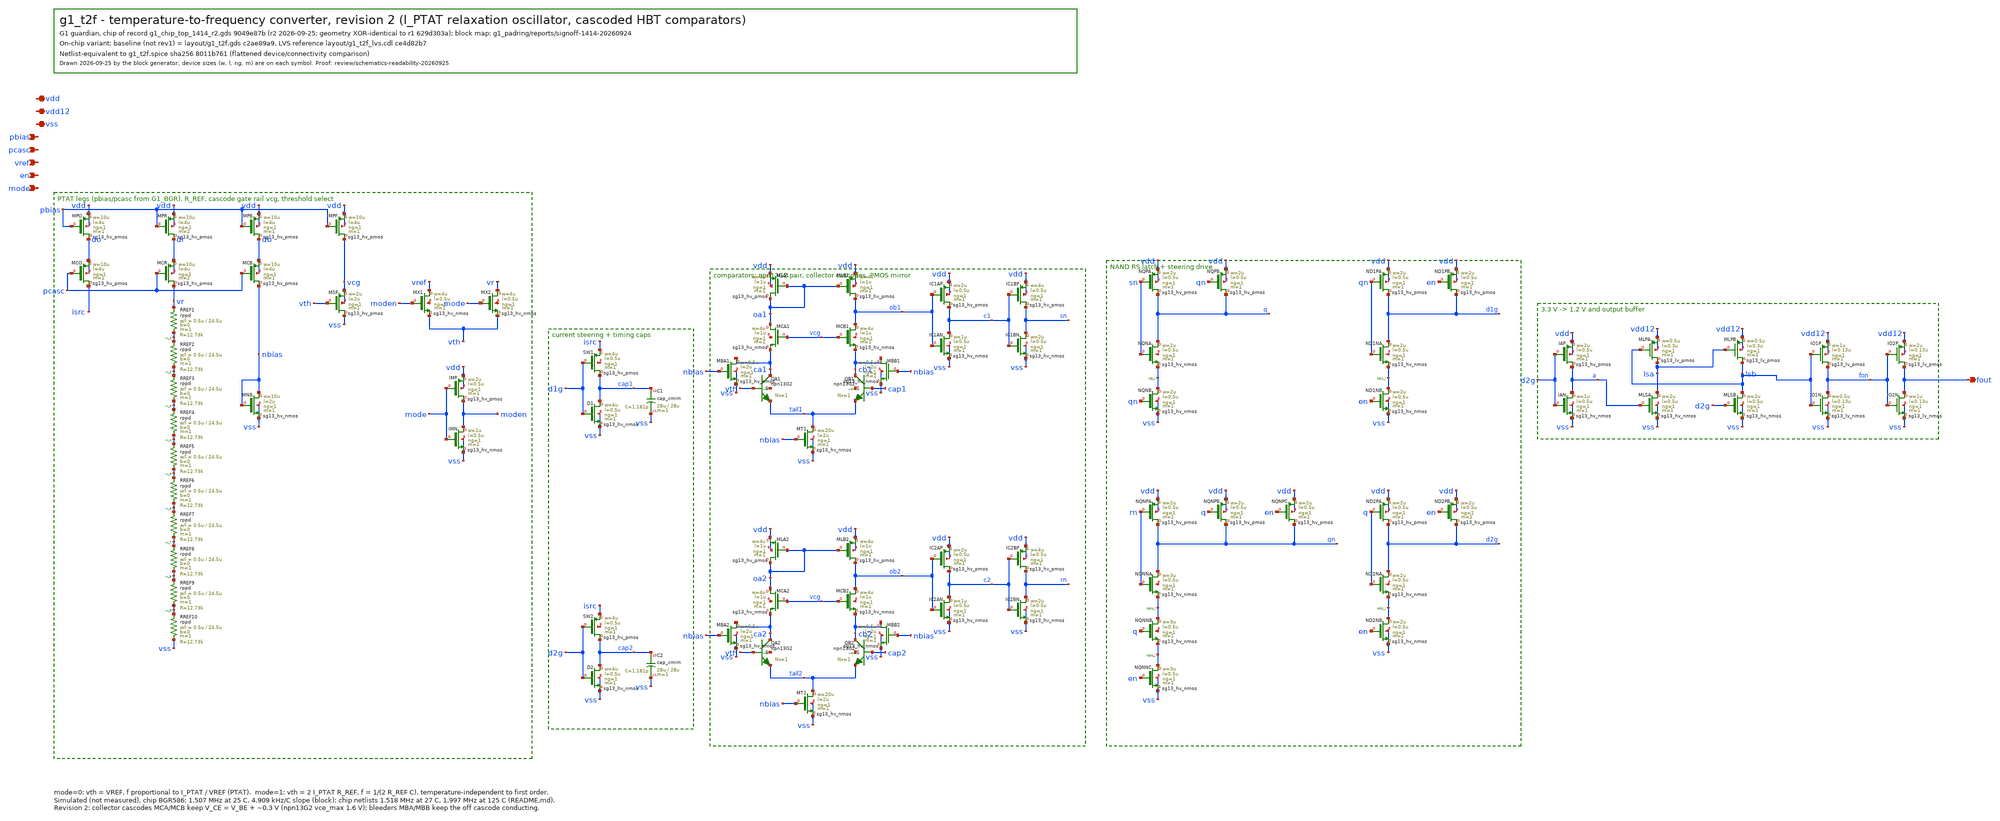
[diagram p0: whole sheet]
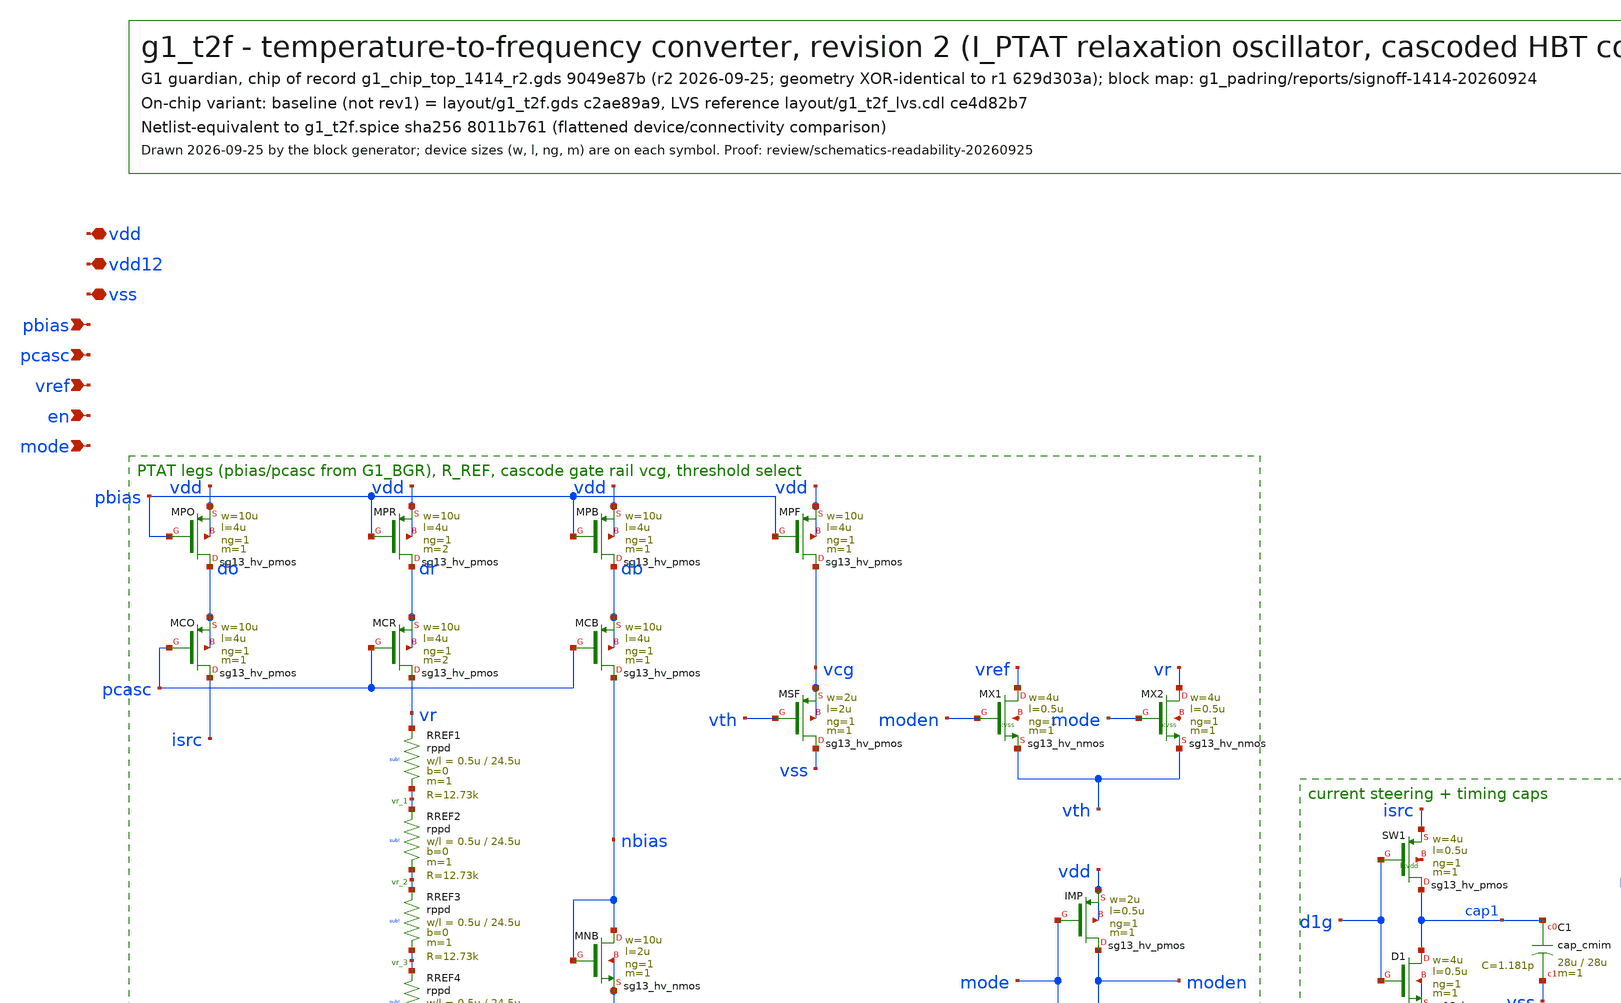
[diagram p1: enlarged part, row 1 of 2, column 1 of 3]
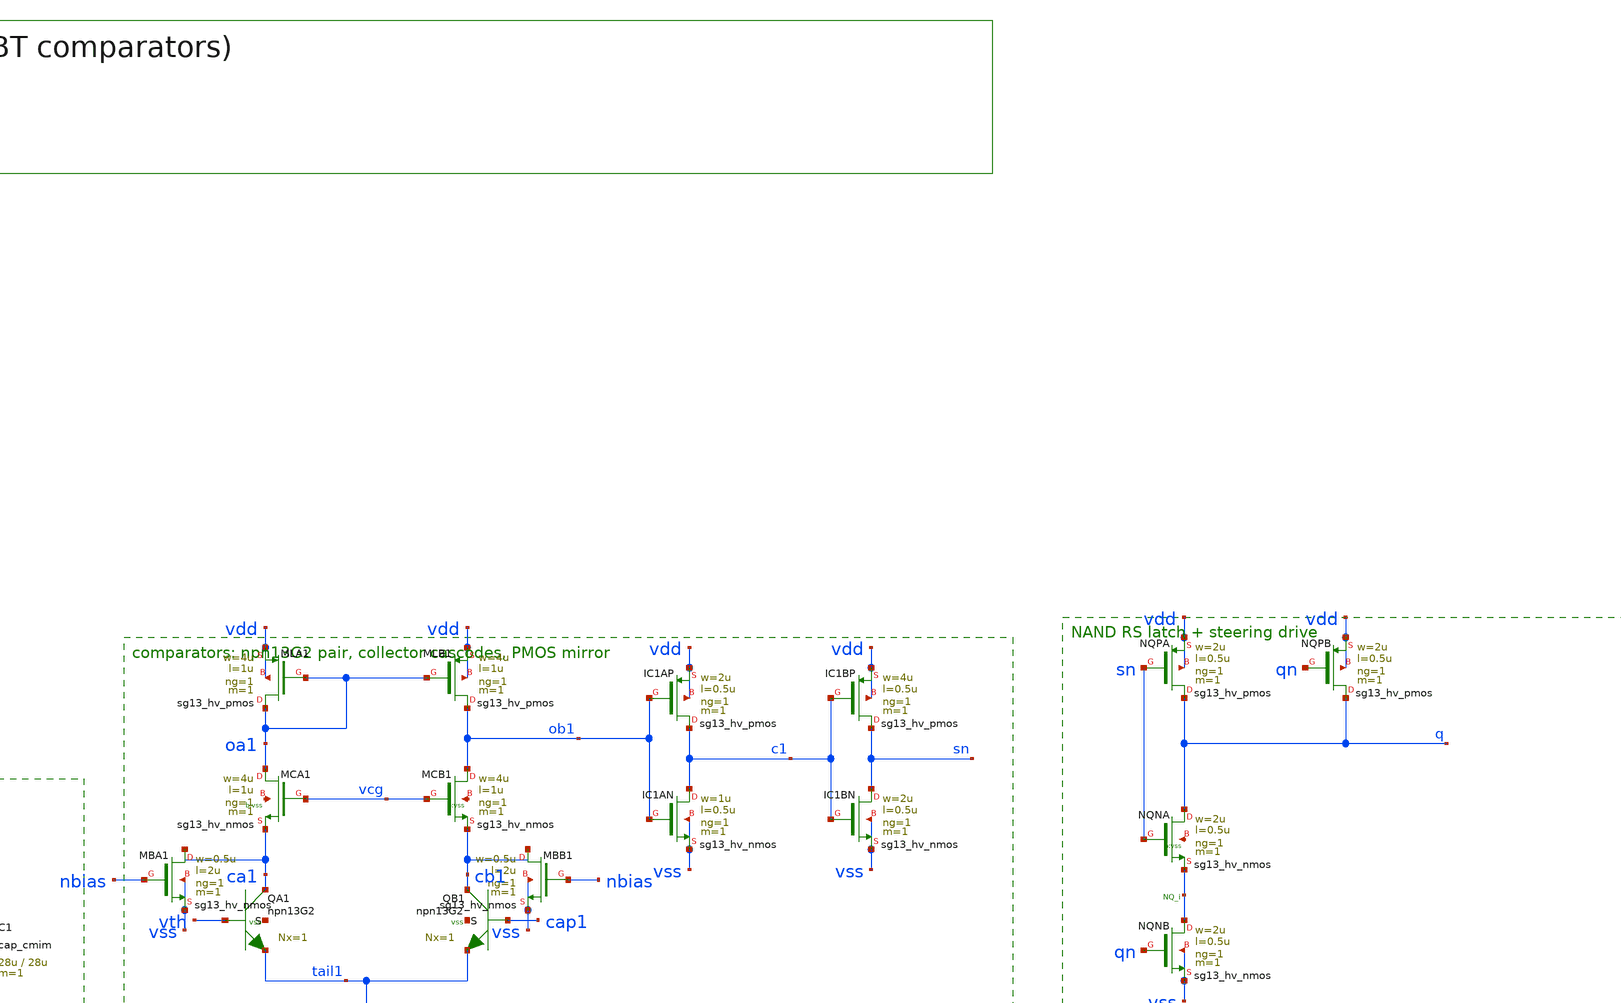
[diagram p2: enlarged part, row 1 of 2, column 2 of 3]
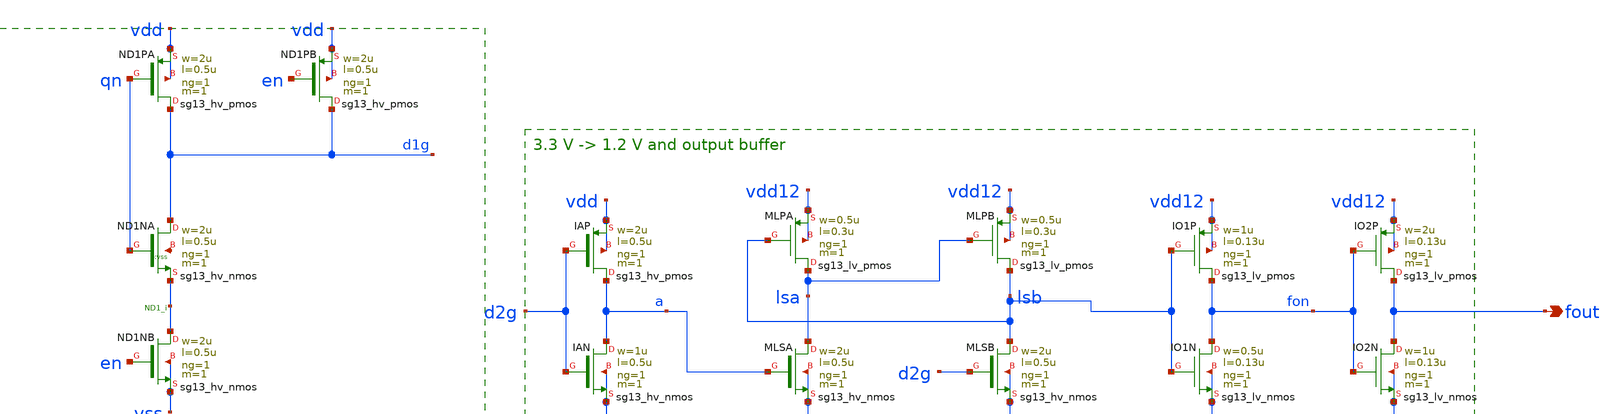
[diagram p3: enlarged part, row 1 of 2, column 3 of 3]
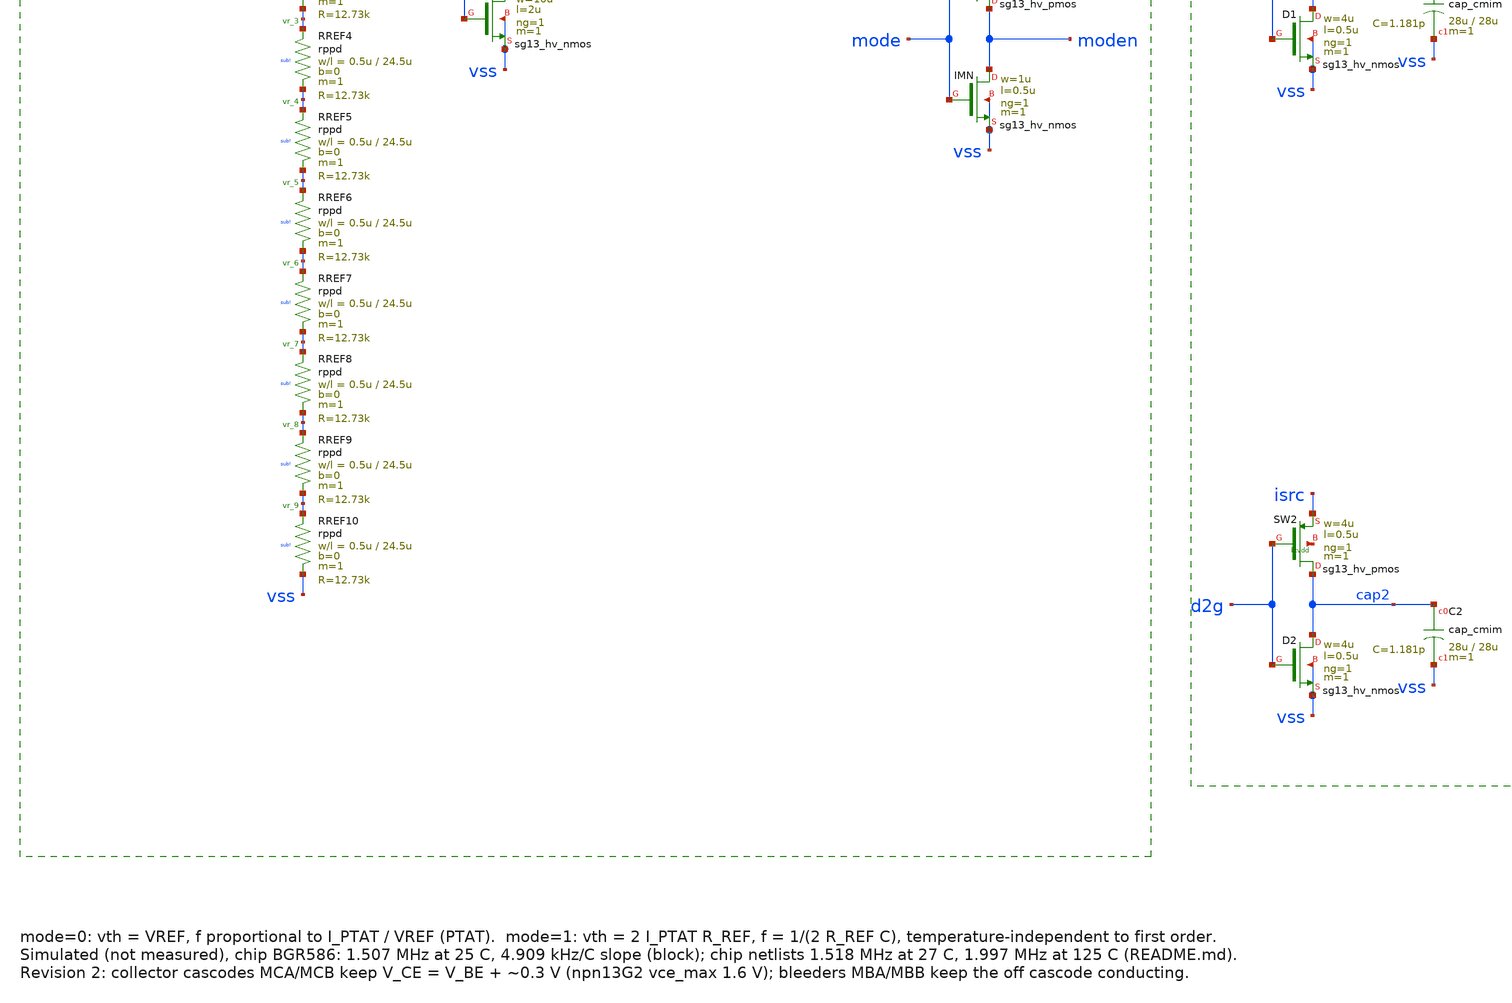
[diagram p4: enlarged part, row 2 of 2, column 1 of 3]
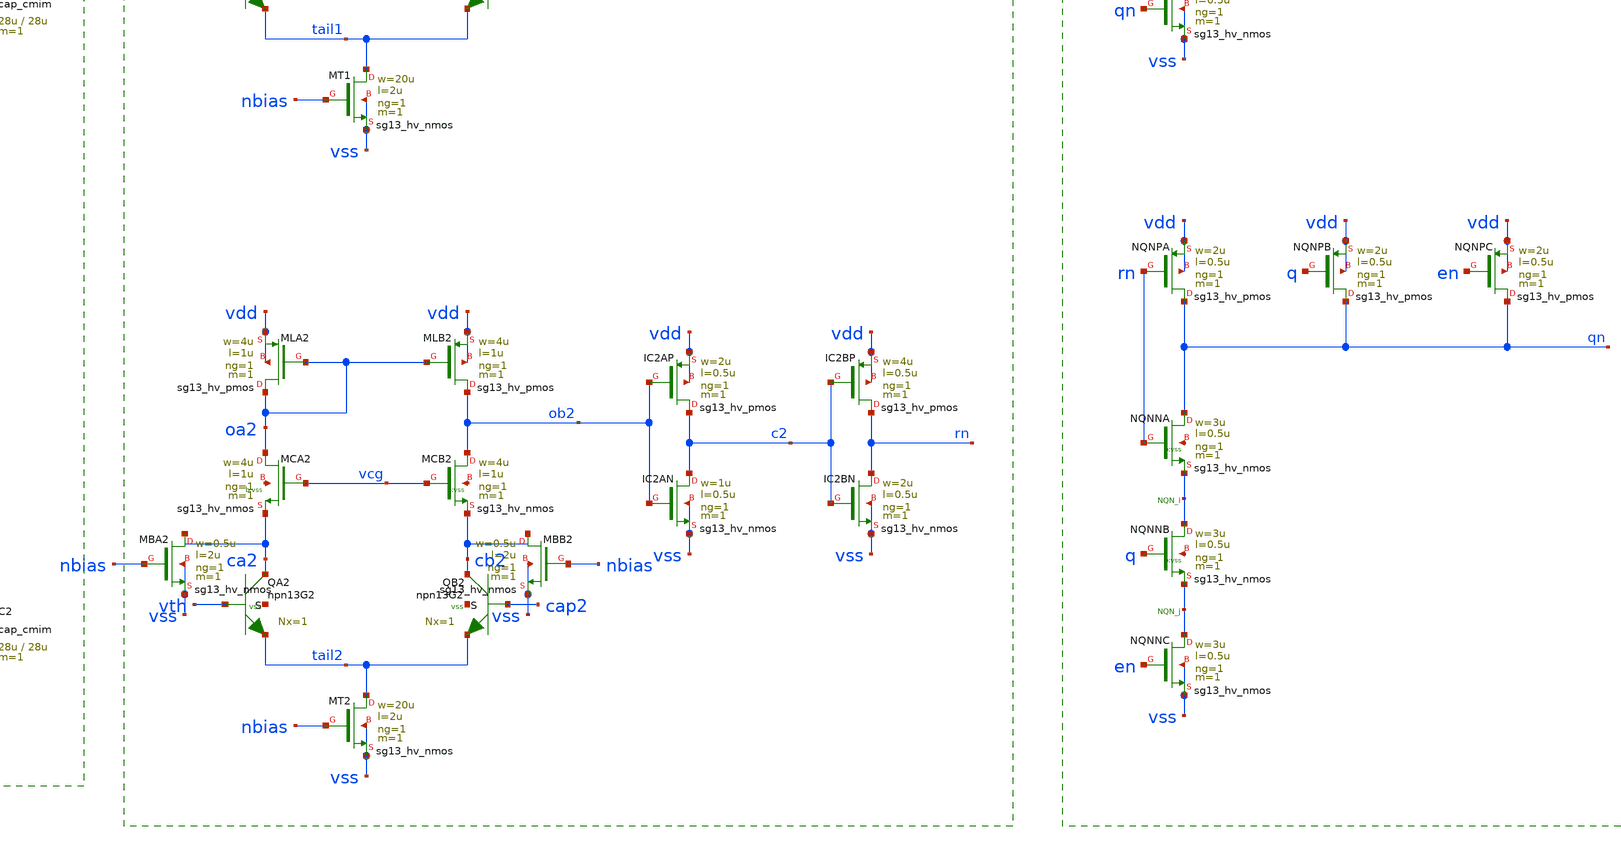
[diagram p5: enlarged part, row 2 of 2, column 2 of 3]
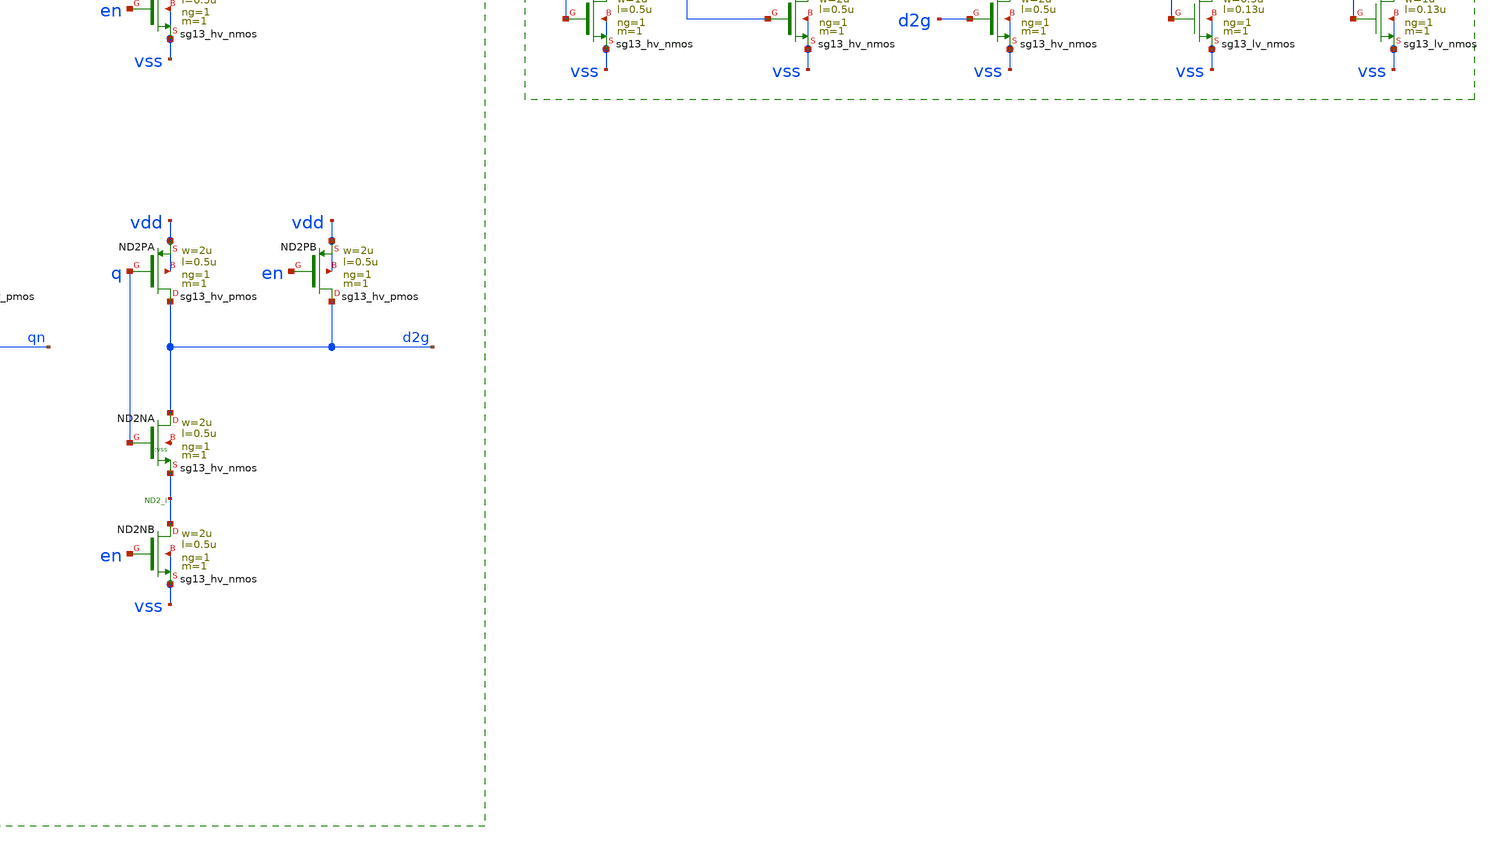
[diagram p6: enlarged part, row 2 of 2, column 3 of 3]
** sch_path: designs/g1-guardian/blocks/g1_t2f/xschem/g1_t2f.sch
**.subckt g1_t2f vdd vdd12 vss pbias pcasc vref en mode fout
*.iopin vdd
*.iopin vdd12
*.iopin vss
*.ipin pbias
*.ipin pcasc
*.ipin vref
*.ipin en
*.ipin mode
*.opin fout
XMPO do pbias vdd vdd sg13_hv_pmos w=10u l=4u ng=1 m=1 mm_ok=1
XMCO isrc pcasc do do sg13_hv_pmos w=10u l=4u ng=1 m=1 mm_ok=1
XMPR dr pbias vdd vdd sg13_hv_pmos w=10u l=4u ng=1 m=2 mm_ok=1
XMCR vr pcasc dr dr sg13_hv_pmos w=10u l=4u ng=1 m=2 mm_ok=1
XRREF1 vr vr_1 sub! rppd w=0.5u l=24.5u m=1 b=0 mm_ok=1
XRREF2 vr_1 vr_2 sub! rppd w=0.5u l=24.5u m=1 b=0 mm_ok=1
XRREF3 vr_2 vr_3 sub! rppd w=0.5u l=24.5u m=1 b=0 mm_ok=1
XRREF4 vr_3 vr_4 sub! rppd w=0.5u l=24.5u m=1 b=0 mm_ok=1
XRREF5 vr_4 vr_5 sub! rppd w=0.5u l=24.5u m=1 b=0 mm_ok=1
XRREF6 vr_5 vr_6 sub! rppd w=0.5u l=24.5u m=1 b=0 mm_ok=1
XRREF7 vr_6 vr_7 sub! rppd w=0.5u l=24.5u m=1 b=0 mm_ok=1
XRREF8 vr_7 vr_8 sub! rppd w=0.5u l=24.5u m=1 b=0 mm_ok=1
XRREF9 vr_8 vr_9 sub! rppd w=0.5u l=24.5u m=1 b=0 mm_ok=1
XRREF10 vr_9 vss sub! rppd w=0.5u l=24.5u m=1 b=0 mm_ok=1
XMPB db pbias vdd vdd sg13_hv_pmos w=10u l=4u ng=1 m=1 mm_ok=1
XMCB nbias pcasc db db sg13_hv_pmos w=10u l=4u ng=1 m=1 mm_ok=1
XMNB nbias nbias vss vss sg13_hv_nmos w=10u l=2u ng=1 m=1 mm_ok=1
XMPF vcg pbias vdd vdd sg13_hv_pmos w=10u l=4u ng=1 m=1 mm_ok=1
XMSF vss vth vcg vcg sg13_hv_pmos w=2u l=2u ng=1 m=1 mm_ok=1
XMX1 vref moden vth vss sg13_hv_nmos w=4u l=0.5u ng=1 m=1 mm_ok=1
XMX2 vr mode vth vss sg13_hv_nmos w=4u l=0.5u ng=1 m=1 mm_ok=1
XIMN moden mode vss vss sg13_hv_nmos w=1u l=0.5u ng=1 m=1 mm_ok=1
XIMP moden mode vdd vdd sg13_hv_pmos w=2u l=0.5u ng=1 m=1 mm_ok=1
XQA1 ca1 vth tail1 vss npn13G2 Nx=1 mm_ok=1
XQB1 cb1 cap1 tail1 vss npn13G2 Nx=1 mm_ok=1
XMCA1 oa1 vcg ca1 vss sg13_hv_nmos w=4u l=1u ng=1 m=1 mm_ok=1
XMCB1 ob1 vcg cb1 vss sg13_hv_nmos w=4u l=1u ng=1 m=1 mm_ok=1
XMBA1 ca1 nbias vss vss sg13_hv_nmos w=0.5u l=2u ng=1 m=1 mm_ok=1
XMBB1 cb1 nbias vss vss sg13_hv_nmos w=0.5u l=2u ng=1 m=1 mm_ok=1
XMLA1 oa1 oa1 vdd vdd sg13_hv_pmos w=4u l=1u ng=1 m=1 mm_ok=1
XMLB1 ob1 oa1 vdd vdd sg13_hv_pmos w=4u l=1u ng=1 m=1 mm_ok=1
XMT1 tail1 nbias vss vss sg13_hv_nmos w=20u l=2u ng=1 m=1 mm_ok=1
XIC1AN c1 ob1 vss vss sg13_hv_nmos w=1u l=0.5u ng=1 m=1 mm_ok=1
XIC1AP c1 ob1 vdd vdd sg13_hv_pmos w=2u l=0.5u ng=1 m=1 mm_ok=1
XIC1BN sn c1 vss vss sg13_hv_nmos w=2u l=0.5u ng=1 m=1 mm_ok=1
XIC1BP sn c1 vdd vdd sg13_hv_pmos w=4u l=0.5u ng=1 m=1 mm_ok=1
XQA2 ca2 vth tail2 vss npn13G2 Nx=1 mm_ok=1
XQB2 cb2 cap2 tail2 vss npn13G2 Nx=1 mm_ok=1
XMCA2 oa2 vcg ca2 vss sg13_hv_nmos w=4u l=1u ng=1 m=1 mm_ok=1
XMCB2 ob2 vcg cb2 vss sg13_hv_nmos w=4u l=1u ng=1 m=1 mm_ok=1
XMBA2 ca2 nbias vss vss sg13_hv_nmos w=0.5u l=2u ng=1 m=1 mm_ok=1
XMBB2 cb2 nbias vss vss sg13_hv_nmos w=0.5u l=2u ng=1 m=1 mm_ok=1
XMLA2 oa2 oa2 vdd vdd sg13_hv_pmos w=4u l=1u ng=1 m=1 mm_ok=1
XMLB2 ob2 oa2 vdd vdd sg13_hv_pmos w=4u l=1u ng=1 m=1 mm_ok=1
XMT2 tail2 nbias vss vss sg13_hv_nmos w=20u l=2u ng=1 m=1 mm_ok=1
XIC2AN c2 ob2 vss vss sg13_hv_nmos w=1u l=0.5u ng=1 m=1 mm_ok=1
XIC2AP c2 ob2 vdd vdd sg13_hv_pmos w=2u l=0.5u ng=1 m=1 mm_ok=1
XIC2BN rn c2 vss vss sg13_hv_nmos w=2u l=0.5u ng=1 m=1 mm_ok=1
XIC2BP rn c2 vdd vdd sg13_hv_pmos w=4u l=0.5u ng=1 m=1 mm_ok=1
XNQPA q sn vdd vdd sg13_hv_pmos w=2u l=0.5u ng=1 m=1 mm_ok=1
XNQPB q qn vdd vdd sg13_hv_pmos w=2u l=0.5u ng=1 m=1 mm_ok=1
XNQNA q sn NQ_i vss sg13_hv_nmos w=2u l=0.5u ng=1 m=1 mm_ok=1
XNQNB NQ_i qn vss vss sg13_hv_nmos w=2u l=0.5u ng=1 m=1 mm_ok=1
XNQNPA qn rn vdd vdd sg13_hv_pmos w=2u l=0.5u ng=1 m=1 mm_ok=1
XNQNPB qn q vdd vdd sg13_hv_pmos w=2u l=0.5u ng=1 m=1 mm_ok=1
XNQNPC qn en vdd vdd sg13_hv_pmos w=2u l=0.5u ng=1 m=1 mm_ok=1
XNQNNA qn rn NQN_i vss sg13_hv_nmos w=3u l=0.5u ng=1 m=1 mm_ok=1
XNQNNB NQN_i q NQN_j vss sg13_hv_nmos w=3u l=0.5u ng=1 m=1 mm_ok=1
XNQNNC NQN_j en vss vss sg13_hv_nmos w=3u l=0.5u ng=1 m=1 mm_ok=1
XND1PA d1g qn vdd vdd sg13_hv_pmos w=2u l=0.5u ng=1 m=1 mm_ok=1
XND1PB d1g en vdd vdd sg13_hv_pmos w=2u l=0.5u ng=1 m=1 mm_ok=1
XND1NA d1g qn ND1_i vss sg13_hv_nmos w=2u l=0.5u ng=1 m=1 mm_ok=1
XND1NB ND1_i en vss vss sg13_hv_nmos w=2u l=0.5u ng=1 m=1 mm_ok=1
XND2PA d2g q vdd vdd sg13_hv_pmos w=2u l=0.5u ng=1 m=1 mm_ok=1
XND2PB d2g en vdd vdd sg13_hv_pmos w=2u l=0.5u ng=1 m=1 mm_ok=1
XND2NA d2g q ND2_i vss sg13_hv_nmos w=2u l=0.5u ng=1 m=1 mm_ok=1
XND2NB ND2_i en vss vss sg13_hv_nmos w=2u l=0.5u ng=1 m=1 mm_ok=1
XSW1 cap1 d1g isrc vdd sg13_hv_pmos w=4u l=0.5u ng=1 m=1 mm_ok=1
XD1 cap1 d1g vss vss sg13_hv_nmos w=4u l=0.5u ng=1 m=1 mm_ok=1
XSW2 cap2 d2g isrc vdd sg13_hv_pmos w=4u l=0.5u ng=1 m=1 mm_ok=1
XD2 cap2 d2g vss vss sg13_hv_nmos w=4u l=0.5u ng=1 m=1 mm_ok=1
XC1 cap1 vss cap_cmim w=28u l=28u m=1 mm_ok=1
XC2 cap2 vss cap_cmim w=28u l=28u m=1 mm_ok=1
XIAN a d2g vss vss sg13_hv_nmos w=1u l=0.5u ng=1 m=1 mm_ok=1
XIAP a d2g vdd vdd sg13_hv_pmos w=2u l=0.5u ng=1 m=1 mm_ok=1
XMLSA lsa a vss vss sg13_hv_nmos w=2u l=0.5u ng=1 m=1 mm_ok=1
XMLSB lsb d2g vss vss sg13_hv_nmos w=2u l=0.5u ng=1 m=1 mm_ok=1
XMLPA lsa lsb vdd12 vdd12 sg13_lv_pmos w=0.5u l=0.3u ng=1 m=1 mm_ok=1
XMLPB lsb lsa vdd12 vdd12 sg13_lv_pmos w=0.5u l=0.3u ng=1 m=1 mm_ok=1
XIO1N fon lsb vss vss sg13_lv_nmos w=0.5u l=0.13u ng=1 m=1 mm_ok=1
XIO1P fon lsb vdd12 vdd12 sg13_lv_pmos w=1u l=0.13u ng=1 m=1 mm_ok=1
XIO2N fout fon vss vss sg13_lv_nmos w=1u l=0.13u ng=1 m=1 mm_ok=1
XIO2P fout fon vdd12 vdd12 sg13_lv_pmos w=2u l=0.13u ng=1 m=1 mm_ok=1
**.ends
.end
